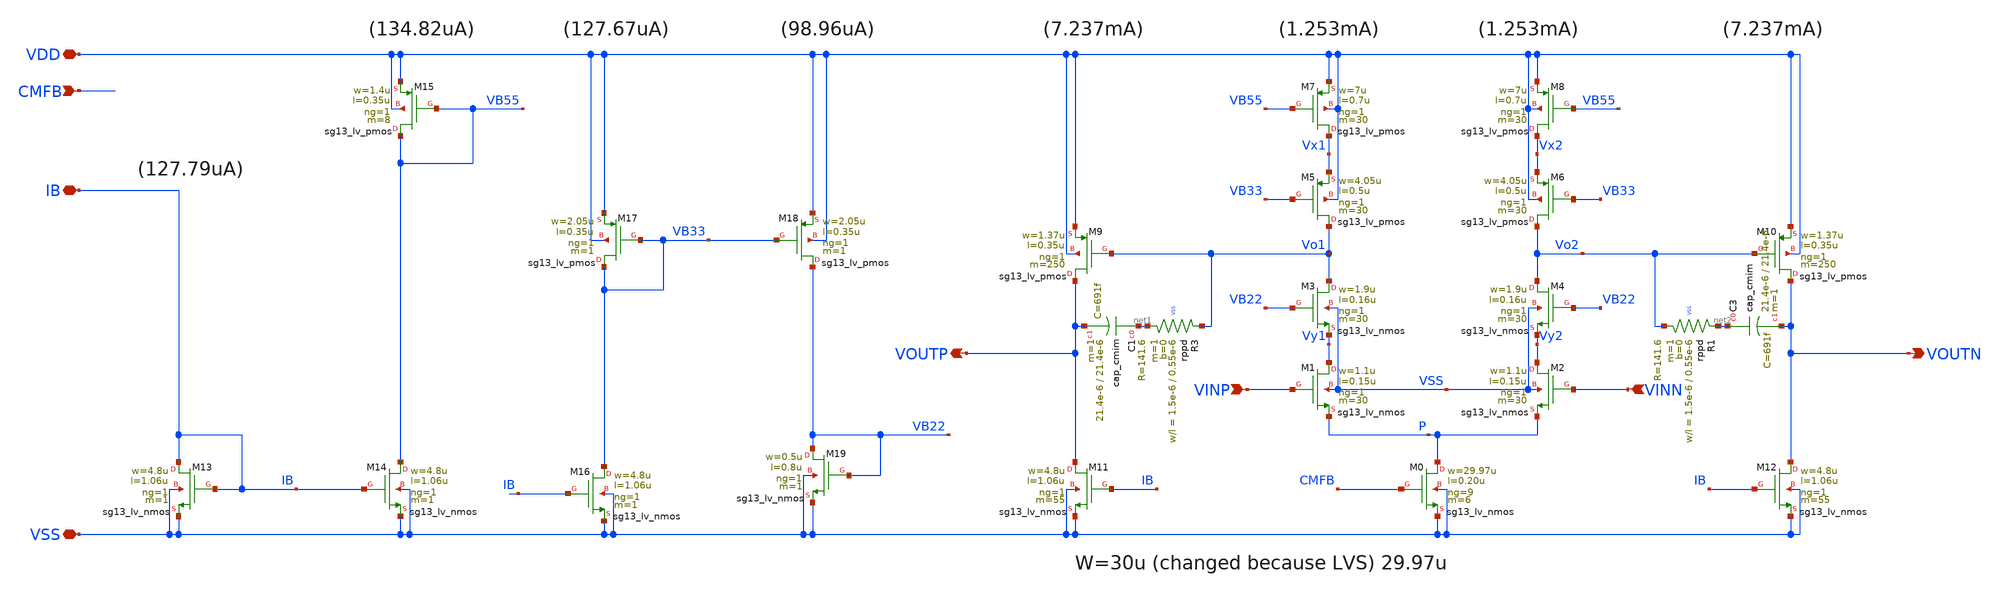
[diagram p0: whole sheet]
** sch_path: OTA_Telescopic_NO_FLATTEN/Schematics_and_Symbols/OTA_Telescopic_core.sch
**.subckt OTA_Telescopic_core VDD VSS VINP VINN VOUTN VOUTP CMFB IB
*.iopin VDD
*.iopin VSS
*.ipin VINP
*.ipin VINN
*.opin VOUTN
*.opin VOUTP
*.ipin CMFB
*.iopin IB
XM15 VB55 VB55 VDD VDD sg13_lv_pmos w=1.4u l=0.35u ng=1 m=8 mm_ok=1
XM17 VB33 VB33 VDD VDD sg13_lv_pmos w=2.05u l=0.35u ng=1 m=1 mm_ok=1
XM18 VB22 VB33 VDD VDD sg13_lv_pmos w=2.05u l=0.35u ng=1 m=1 mm_ok=1
XM9 VOUTP Vo1 VDD VDD sg13_lv_pmos w=1.37u l=0.35u ng=1 m=250 mm_ok=1
XM7 Vx1 VB55 VDD VDD sg13_lv_pmos w=7u l=0.7u ng=1 m=30 mm_ok=1
XM5 Vo1 VB33 Vx1 VDD sg13_lv_pmos w=4.05u l=0.5u ng=1 m=30 mm_ok=1
XM8 Vx2 VB55 VDD VDD sg13_lv_pmos w=7u l=0.7u ng=1 m=30 mm_ok=1
XM6 Vo2 VB33 Vx2 VDD sg13_lv_pmos w=4.05u l=0.5u ng=1 m=30 mm_ok=1
XM10 VOUTN Vo2 VDD VDD sg13_lv_pmos w=1.37u l=0.35u ng=1 m=250 mm_ok=1
XM13 IB IB VSS VSS sg13_lv_nmos w=4.8u l=1.06u ng=1 m=1 mm_ok=1
XM14 VB55 IB VSS VSS sg13_lv_nmos w=4.8u l=1.06u ng=1 m=1 mm_ok=1
XM16 VB33 IB VSS VSS sg13_lv_nmos w=4.8u l=1.06u ng=1 m=1 mm_ok=1
XM19 VB22 VB22 VSS VSS sg13_lv_nmos w=0.5u l=0.8u ng=1 m=1 mm_ok=1
XM11 VOUTP IB VSS VSS sg13_lv_nmos w=4.8u l=1.06u ng=1 m=55 mm_ok=1
XM0 P CMFB VSS VSS sg13_lv_nmos w=29.97u l=0.20u ng=9 m=6 mm_ok=1
XM3 Vo1 VB22 Vy1 VSS sg13_lv_nmos w=1.9u l=0.16u ng=1 m=30 mm_ok=1
XM1 Vy1 VINP P VSS sg13_lv_nmos w=1.1u l=0.15u ng=1 m=30 mm_ok=1
XM4 Vo2 VB22 Vy2 VSS sg13_lv_nmos w=1.9u l=0.16u ng=1 m=30 mm_ok=1
XM2 Vy2 VINN P VSS sg13_lv_nmos w=1.1u l=0.15u ng=1 m=30 mm_ok=1
XM12 VOUTN IB VSS VSS sg13_lv_nmos w=4.8u l=1.06u ng=1 m=55 mm_ok=1
XR3 Vo1 net1 VSS rppd w=1.5e-6 l=0.55e-6 m=1 b=0 mm_ok=1
XR1 net2 Vo2 VSS rppd w=1.5e-6 l=0.55e-6 m=1 b=0 mm_ok=1
XC3 net2 VOUTN cap_cmim w=21.4e-6 l=21.4e-6 m=1 mm_ok=1
XC1 net1 VOUTP cap_cmim w=21.4e-6 l=21.4e-6 m=1 mm_ok=1
**.ends
.end
